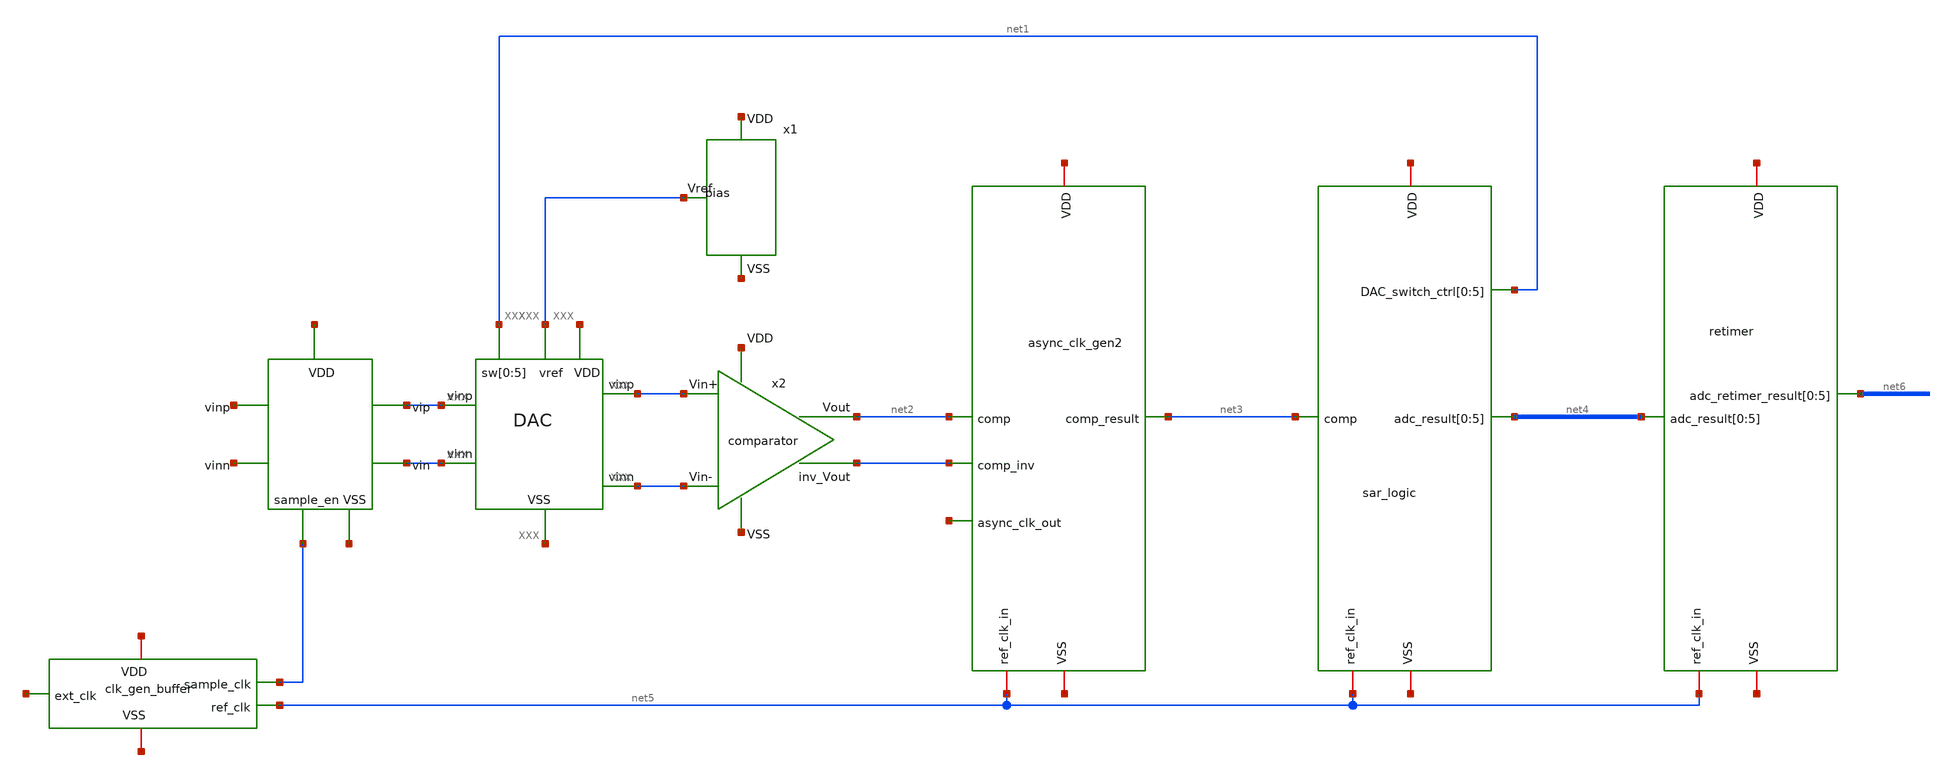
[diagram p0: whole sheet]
** sch_path: just_sym/6bit_SAR_ADC_top.sch
**.subckt 6bit_SAR_ADC_top
x1 net1 DAC
x1 VGND VNB VPB VPWR sky130_fd_sc_hd__a21boi_0
x2 net1 net1 net14 net15 net2
x1 net16 net17 net2 net2 net3 net18 net5 async_clk_gen2
**.ends
.end
